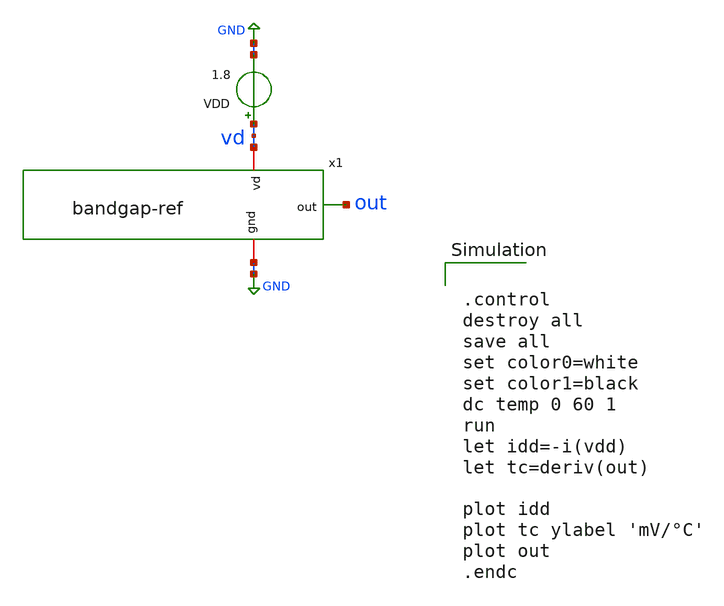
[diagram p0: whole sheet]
** sch_path: bandgap-ref/xschem/bandgap-ref_tb-temp.sch
**.subckt bandgap-ref_tb-temp
VDD vd GND 1.8
x1 vd out GND bandgap-ref
**** begin user architecture code


.control
destroy all
save all
set color0=white
set color1=black
dc temp 0 60 1
run
let idd=-i(vdd)
let tc=deriv(out)

plot idd
plot tc ylabel 'mV/°C'
plot out
.endc


 .lib $::SKYWATER_MODELS/sky130.lib.spice tt
.include $::SKYWATER_STDCELLS/sky130_fd_sc_hd.spice

**** end user architecture code
**.ends

* expanding   symbol:  /home/hugodg/projects-sky130/temp-sensor/bandgap-ref/xschem/bandgap-ref.sym #
*+ of pins=3
** sym_path: bandgap-ref/xschem/bandgap-ref.sym
** sch_path: bandgap-ref/xschem/bandgap-ref.sch
.subckt bandgap-ref vd out gnd
*.iopin vd
*.iopin gnd
*.opin out
XMN1 net4 net4 gnd gnd sky130_fd_pr__nfet_01v8 L=4 W=60 nf=1 ad='int((nf+1)/2) * W/nf * 0.29' as='int((nf+2)/2) * W/nf * 0.29'
+ pd='2*int((nf+1)/2) * (W/nf + 0.29)' ps='2*int((nf+2)/2) * (W/nf + 0.29)' nrd='0.29 / W' nrs='0.29 / W'
+ sa=0 sb=0 sd=0 mult=1 m=1
XMP1 net4 net1 vd vd sky130_fd_pr__pfet_01v8 L=4 W=5 nf=1 ad='int((nf+1)/2) * W/nf * 0.29' as='int((nf+2)/2) * W/nf * 0.29'
+ pd='2*int((nf+1)/2) * (W/nf + 0.29)' ps='2*int((nf+2)/2) * (W/nf + 0.29)' nrd='0.29 / W' nrs='0.29 / W'
+ sa=0 sb=0 sd=0 mult=1 m=1
XMP2 net2 net1 vd vd sky130_fd_pr__pfet_01v8 L=4 W=5 nf=1 ad='int((nf+1)/2) * W/nf * 0.29' as='int((nf+2)/2) * W/nf * 0.29'
+ pd='2*int((nf+1)/2) * (W/nf + 0.29)' ps='2*int((nf+2)/2) * (W/nf + 0.29)' nrd='0.29 / W' nrs='0.29 / W'
+ sa=0 sb=0 sd=0 mult=1 m=1
XMP3 out net2 vd vd sky130_fd_pr__pfet_01v8 L=4 W=5 nf=1 ad='int((nf+1)/2) * W/nf * 0.29' as='int((nf+2)/2) * W/nf * 0.29'
+ pd='2*int((nf+1)/2) * (W/nf + 0.29)' ps='2*int((nf+2)/2) * (W/nf + 0.29)' nrd='0.29 / W' nrs='0.29 / W'
+ sa=0 sb=0 sd=0 mult=1 m=1
XMN2 net2 net4 net3 gnd sky130_fd_pr__nfet_01v8 L=4 W=87 nf=1 ad='int((nf+1)/2) * W/nf * 0.29' as='int((nf+2)/2) * W/nf * 0.29'
+ pd='2*int((nf+1)/2) * (W/nf + 0.29)' ps='2*int((nf+2)/2) * (W/nf + 0.29)' nrd='0.29 / W' nrs='0.29 / W'
+ sa=0 sb=0 sd=0 mult=1 m=1
XMN3 out out gnd gnd sky130_fd_pr__nfet_01v8 L=50 W=3 nf=1 ad='int((nf+1)/2) * W/nf * 0.29' as='int((nf+2)/2) * W/nf * 0.29'
+ pd='2*int((nf+1)/2) * (W/nf + 0.29)' ps='2*int((nf+2)/2) * (W/nf + 0.29)' nrd='0.29 / W' nrs='0.29 / W'
+ sa=0 sb=0 sd=0 mult=1 m=1
XMN4 net3 out gnd gnd sky130_fd_pr__nfet_01v8 L=10 W=3 nf=1 ad='int((nf+1)/2) * W/nf * 0.29' as='int((nf+2)/2) * W/nf * 0.29'
+ pd='2*int((nf+1)/2) * (W/nf + 0.29)' ps='2*int((nf+2)/2) * (W/nf + 0.29)' nrd='0.29 / W' nrs='0.29 / W'
+ sa=0 sb=0 sd=0 mult=1 m=1
XMS1 net1 net5 gnd gnd sky130_fd_pr__nfet_01v8 L=3 W=30 nf=1 ad='int((nf+1)/2) * W/nf * 0.29' as='int((nf+2)/2) * W/nf * 0.29'
+ pd='2*int((nf+1)/2) * (W/nf + 0.29)' ps='2*int((nf+2)/2) * (W/nf + 0.29)' nrd='0.29 / W' nrs='0.29 / W'
+ sa=0 sb=0 sd=0 mult=1 m=1
XMD3 net5 net5 vd vd sky130_fd_pr__pfet_01v8 L=3 W=3 nf=1 ad='int((nf+1)/2) * W/nf * 0.29' as='int((nf+2)/2) * W/nf * 0.29'
+ pd='2*int((nf+1)/2) * (W/nf + 0.29)' ps='2*int((nf+2)/2) * (W/nf + 0.29)' nrd='0.29 / W' nrs='0.29 / W'
+ sa=0 sb=0 sd=0 mult=1 m=1
XMD2 net6 net6 net5 net5 sky130_fd_pr__pfet_01v8 L=3 W=3 nf=1 ad='int((nf+1)/2) * W/nf * 0.29' as='int((nf+2)/2) * W/nf * 0.29'
+ pd='2*int((nf+1)/2) * (W/nf + 0.29)' ps='2*int((nf+2)/2) * (W/nf + 0.29)' nrd='0.29 / W' nrs='0.29 / W'
+ sa=0 sb=0 sd=0 mult=1 m=1
XMD1 net6 net6 gnd gnd sky130_fd_pr__nfet_01v8 L=3 W=3 nf=1 ad='int((nf+1)/2) * W/nf * 0.29' as='int((nf+2)/2) * W/nf * 0.29'
+ pd='2*int((nf+1)/2) * (W/nf + 0.29)' ps='2*int((nf+2)/2) * (W/nf + 0.29)' nrd='0.29 / W' nrs='0.29 / W'
+ sa=0 sb=0 sd=0 mult=1 m=1
XMS2 vd net6 net4 gnd sky130_fd_pr__nfet_01v8 L=3 W=30 nf=1 ad='int((nf+1)/2) * W/nf * 0.29' as='int((nf+2)/2) * W/nf * 0.29'
+ pd='2*int((nf+1)/2) * (W/nf + 0.29)' ps='2*int((nf+2)/2) * (W/nf + 0.29)' nrd='0.29 / W' nrs='0.29 / W'
+ sa=0 sb=0 sd=0 mult=1 m=1
.ends

.GLOBAL GND
.end
